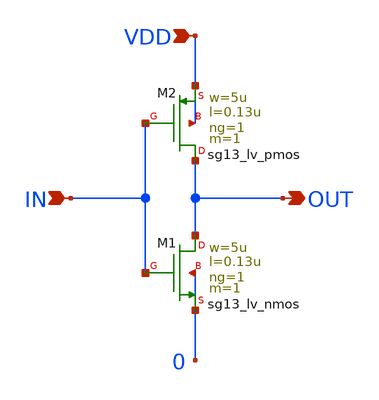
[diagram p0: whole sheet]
** sch_path: demo/cosim/test_new/vacask_cosim_hier/final_folder/ainv.sch
**.subckt ainv IN OUT VDD
*.ipin IN
*.opin OUT
*.ipin VDD
XM1 OUT IN 0 0 sg13_lv_nmos w=5u l=0.13u ng=1 m=1 mm_ok=1
XM2 OUT IN VDD VDD sg13_lv_pmos w=5u l=0.13u ng=1 m=1 mm_ok=1
**.ends
.end
